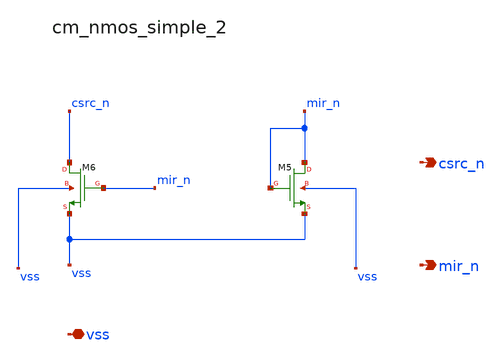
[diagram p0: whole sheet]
** sch_path: analog-db/raw/amp_025_hsu_classab_ota/hier/blocks/cm_nmos_simple_2.sch
**.subckt cm_nmos_simple_2 vss csrc_n mir_n
*.iopin vss
*.opin csrc_n
*.opin mir_n
XM5 mir_n mir_n vss vss sg13_lv_nmos w=x_dut_xm5_w l=x_dut_xm5_l ng=1 m=x_dut_xm5_m
XM6 csrc_n mir_n vss vss sg13_lv_nmos w=x_dut_xm6_w l=x_dut_xm6_l ng=1 m=x_dut_xm6_m
**.ends
.end
